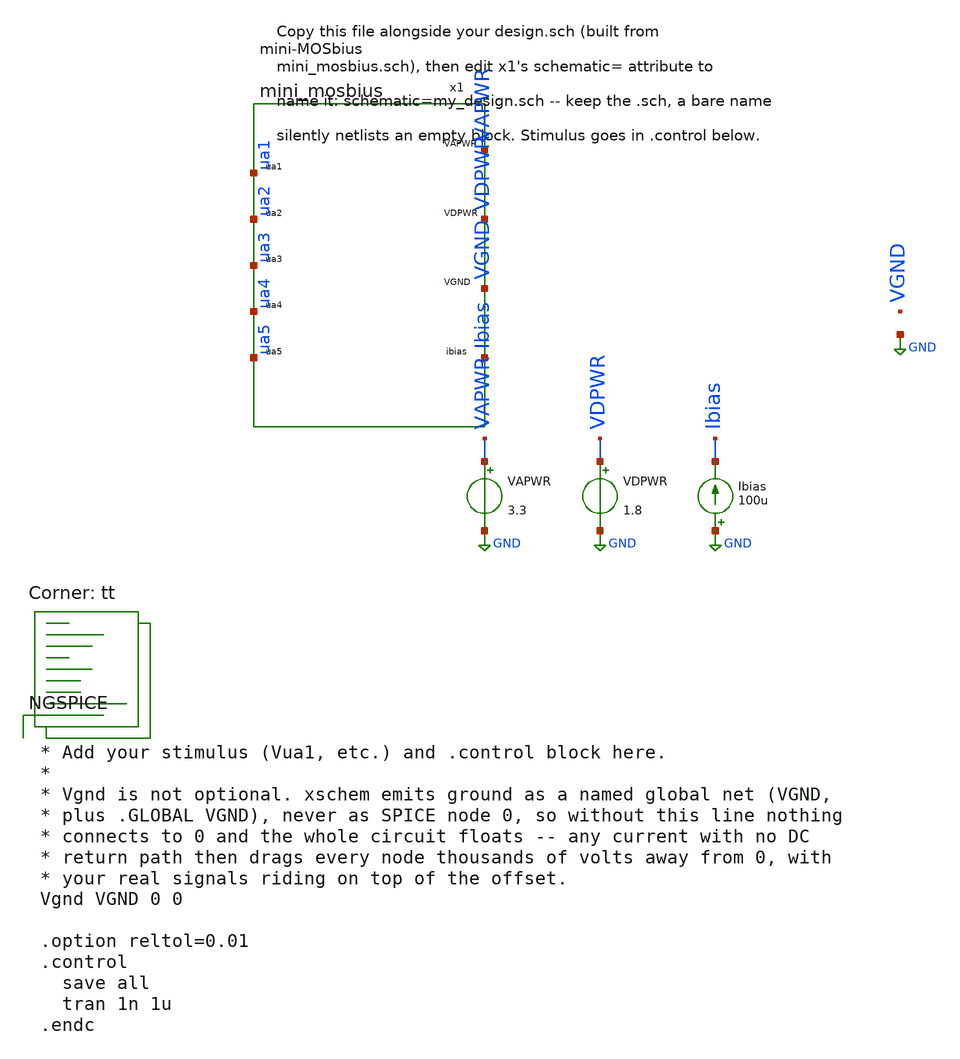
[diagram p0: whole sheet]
** sch_path: xschem/mosbius_lib/tb_template.sch
**.subckt tb_template
x1 Ibias ua1 ua2 ua3 ua4 ua5 VAPWR VDPWR VGND mini_mosbius
VAPWR VAPWR GND 3.3
VDPWR VDPWR GND 1.8
Ibias GND Ibias 100u
**** begin user architecture code
.lib $::SKYWATER_MODELS/sky130.lib.spice tt


* Add your stimulus (Vua1, etc.) and .control block here.
*
* Vgnd is not optional. xschem emits ground as a named global net (VGND,
* plus .GLOBAL VGND), never as SPICE node 0, so without this line nothing
* connects to 0 and the whole circuit floats -- any current with no DC
* return path then drags every node thousands of volts away from 0, with
* your real signals riding on top of the offset.
Vgnd VGND 0 0

.option reltol=0.01
.control
  save all
  tran 1n 1u
.endc


**** end user architecture code
**.ends

* expanding   symbol:  mini_mosbius.sym # of pins=9
** sym_path: xschem/mosbius_lib/mini_mosbius.sym
** sch_path: xschem/mosbius_lib/mini_mosbius.sch
.subckt mini_mosbius ibias ua1 ua2 ua3 ua4 ua5 VAPWR VDPWR VGND
*.iopin ibias
*.iopin ua1
*.iopin ua2
*.iopin ua3
*.iopin ua4
*.iopin ua5
*.iopin VAPWR
*.iopin VDPWR
*.iopin VGND
.ends

.GLOBAL GND
.end
